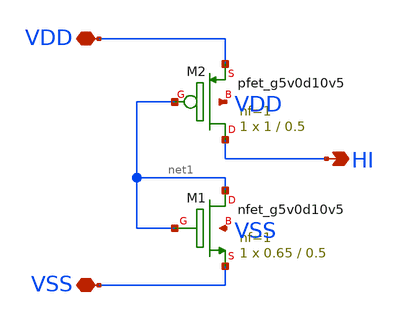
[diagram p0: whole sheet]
** sch_path: xschem/tie_high.sch
**.subckt tie_high VSS VDD HI
*.iopin VSS
*.iopin VDD
*.opin HI
XM1 net1 net1 VSS VSS sky130_fd_pr__nfet_g5v0d10v5 L=0.5 W=0.65 nf=1 ad='int((1 + 1)/2) * 0.65 / 1 * 0.29'
+ as='int((1 + 2)/2) * 0.65 / 1 * 0.29' pd='2*int((1 + 1)/2) * (0.65 / 1 + 0.29)' ps='2*int((1 + 2)/2) * (0.65 / 1 + 0.29)'
+ nrd='0.29 / 0.65 ' nrs='0.29 / 0.65 ' sa=0 sb=0 sd=0 mult=1 m=1
XM2 HI net1 VDD VDD sky130_fd_pr__pfet_g5v0d10v5 L=0.5 W=1 nf=1 ad='int((1 + 1)/2) * 1 / 1 * 0.29' as='int((1 + 2)/2) * 1 / 1 * 0.29'
+ pd='2*int((1 + 1)/2) * (1 / 1 + 0.29)' ps='2*int((1 + 2)/2) * (1 / 1 + 0.29)' nrd='0.29 / 1 ' nrs='0.29 / 1 '
+ sa=0 sb=0 sd=0 mult=1 m=1
**.ends
.end
